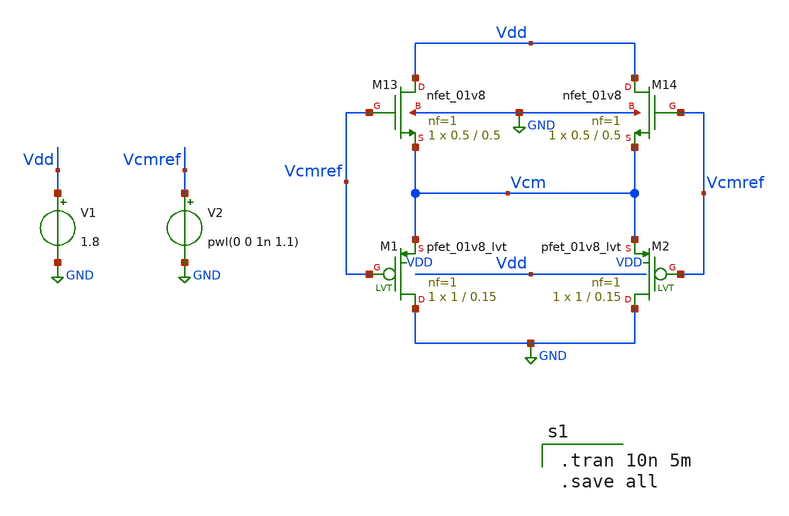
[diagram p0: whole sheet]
** sch_path: xschem/xschemfiles/buffertest.sch
**.subckt buffertest
XM13 Vdd Vcmref Vcm GND sky130_fd_pr__nfet_01v8 L=0.5 W=0.5 nf=1 ad='int((nf+1)/2) * W/nf * 0.29' as='int((nf+2)/2) * W/nf * 0.29'
+ pd='2*int((nf+1)/2) * (W/nf + 0.29)' ps='2*int((nf+2)/2) * (W/nf + 0.29)' nrd='0.29 / W' nrs='0.29 / W'
+ sa=0 sb=0 sd=0 mult=1 m=1
XM14 Vdd Vcmref Vcm GND sky130_fd_pr__nfet_01v8 L=0.5 W=0.5 nf=1 ad='int((nf+1)/2) * W/nf * 0.29' as='int((nf+2)/2) * W/nf * 0.29'
+ pd='2*int((nf+1)/2) * (W/nf + 0.29)' ps='2*int((nf+2)/2) * (W/nf + 0.29)' nrd='0.29 / W' nrs='0.29 / W'
+ sa=0 sb=0 sd=0 mult=1 m=1
V2 Vcmref GND pwl(0 0 1n 1.1)
V1 Vdd GND 1.8
XM1 GND Vcmref Vcm VDD sky130_fd_pr__pfet_01v8_lvt L=0.15 W=1 nf=1 ad='int((nf+1)/2) * W/nf * 0.29' as='int((nf+2)/2) * W/nf * 0.29'
+ pd='2*int((nf+1)/2) * (W/nf + 0.29)' ps='2*int((nf+2)/2) * (W/nf + 0.29)' nrd='0.29 / W' nrs='0.29 / W'
+ sa=0 sb=0 sd=0 mult=1 m=1
XM2 GND Vcmref Vcm VDD sky130_fd_pr__pfet_01v8_lvt L=0.15 W=1 nf=1 ad='int((nf+1)/2) * W/nf * 0.29' as='int((nf+2)/2) * W/nf * 0.29'
+ pd='2*int((nf+1)/2) * (W/nf + 0.29)' ps='2*int((nf+2)/2) * (W/nf + 0.29)' nrd='0.29 / W' nrs='0.29 / W'
+ sa=0 sb=0 sd=0 mult=1 m=1
**** begin user architecture code

.tran 10n 5m
.save all


** opencircuitdesign pdks install
.lib $::SKYWATER_MODELS/sky130.lib.spice tt


**** end user architecture code
**.ends
.GLOBAL GND
.end
